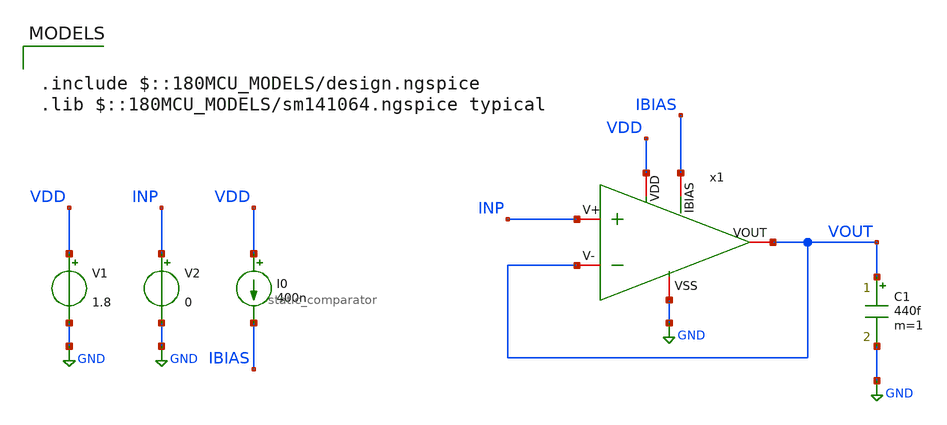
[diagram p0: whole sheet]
** sch_path: designs/static_comparator/xschem/static_comparator_tb_offset.sch
**.subckt static_comparator_tb_offset
V1 VDD GND 1.8
V2 INP GND 0
C1 VOUT GND 440f m=1
I0 VDD IBIAS 400n
x1 VDD IBIAS GND INP VOUT VOUT static_comparator
**** begin user architecture code

.include $::180MCU_MODELS/design.ngspice
.lib $::180MCU_MODELS/sm141064.ngspice typical




.control
save all

**Simulations
op
dc v2 0 1.8 0.01

**Plots
setplot dc1
let VIN = V(INP)
let VOUT = V(VOUT)
plot VOUT

meas dc vout_at_v2_0 find v(VOUT) when v2 = 0

setplot op1
write static_comparator_tb_offset.raw
.endc


**** end user architecture code
**.ends
.GLOBAL GND
.end
